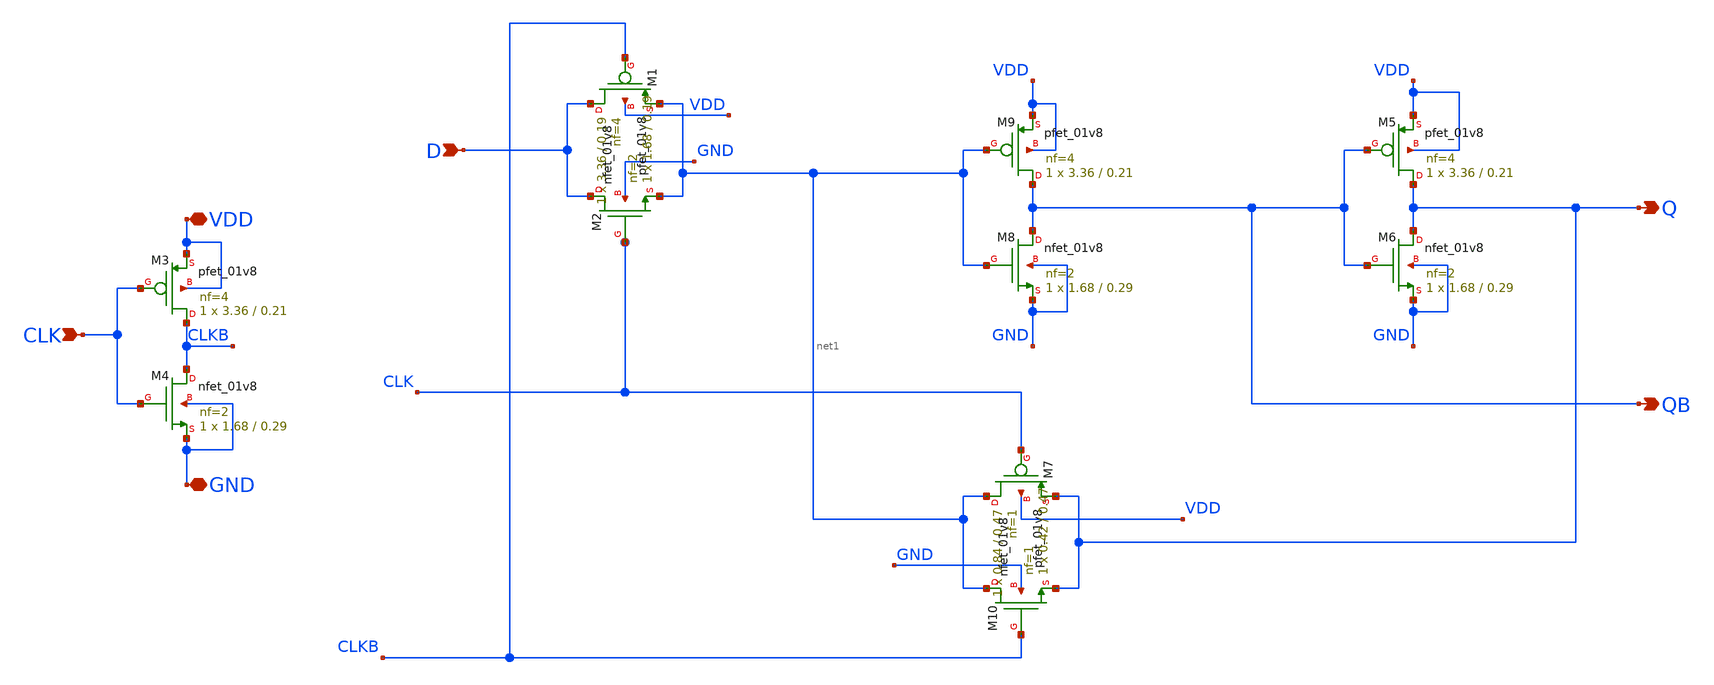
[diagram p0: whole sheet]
** sch_path: cells/DLX4/schematic/dlx4.sch
**.subckt dlx4 D VDD GND CLK QB Q
*.ipin D
*.iopin VDD
*.iopin GND
*.ipin CLK
*.opin QB
*.opin Q
XM1 D CLKB net1 VDD sky130_fd_pr__pfet_01v8 L=0.19 W=3.36 nf=4 ad='int((4 + 1)/2) * 3.36 / 4 * 0.29'
+ as='int((4 + 2)/2) * 3.36 / 4 * 0.29' pd='2*int((4 + 1)/2) * (3.36 / 4 + 0.29)' ps='2*int((4 + 2)/2) * (3.36 / 4 + 0.29)'
+ nrd='0.29 / 3.36 ' nrs='0.29 / 3.36 ' sa=0 sb=0 sd=0 mult=1 m=1
XM2 D CLK net1 GND sky130_fd_pr__nfet_01v8 L=0.19 W=1.68 nf=2 ad='int((2 + 1)/2) * 1.68 / 2 * 0.29' as='int((2 + 2)/2) * 1.68 / 2 * 0.29'
+ pd='2*int((2 + 1)/2) * (1.68 / 2 + 0.29)' ps='2*int((2 + 2)/2) * (1.68 / 2 + 0.29)' nrd='0.29 / 1.68 '
+ nrs='0.29 / 1.68 ' sa=0 sb=0 sd=0 mult=1 m=1
XM3 CLKB CLK VDD VDD sky130_fd_pr__pfet_01v8 L=0.21 W=3.36 nf=4 ad='int((4 + 1)/2) * 3.36 / 4 * 0.29'
+ as='int((4 + 2)/2) * 3.36 / 4 * 0.29' pd='2*int((4 + 1)/2) * (3.36 / 4 + 0.29)' ps='2*int((4 + 2)/2) * (3.36 / 4 + 0.29)'
+ nrd='0.29 / 3.36 ' nrs='0.29 / 3.36 ' sa=0 sb=0 sd=0 mult=1 m=1
XM4 CLKB CLK GND GND sky130_fd_pr__nfet_01v8 L=0.29 W=1.68 nf=2 ad='int((2 + 1)/2) * 1.68 / 2 * 0.29'
+ as='int((2 + 2)/2) * 1.68 / 2 * 0.29' pd='2*int((2 + 1)/2) * (1.68 / 2 + 0.29)' ps='2*int((2 + 2)/2) * (1.68 / 2 + 0.29)'
+ nrd='0.29 / 1.68 ' nrs='0.29 / 1.68 ' sa=0 sb=0 sd=0 mult=1 m=1
XM9 QB net1 VDD VDD sky130_fd_pr__pfet_01v8 L=0.21 W=3.36 nf=4 ad='int((4 + 1)/2) * 3.36 / 4 * 0.29'
+ as='int((4 + 2)/2) * 3.36 / 4 * 0.29' pd='2*int((4 + 1)/2) * (3.36 / 4 + 0.29)' ps='2*int((4 + 2)/2) * (3.36 / 4 + 0.29)'
+ nrd='0.29 / 3.36 ' nrs='0.29 / 3.36 ' sa=0 sb=0 sd=0 mult=1 m=1
XM8 QB net1 GND GND sky130_fd_pr__nfet_01v8 L=0.29 W=1.68 nf=2 ad='int((2 + 1)/2) * 1.68 / 2 * 0.29'
+ as='int((2 + 2)/2) * 1.68 / 2 * 0.29' pd='2*int((2 + 1)/2) * (1.68 / 2 + 0.29)' ps='2*int((2 + 2)/2) * (1.68 / 2 + 0.29)'
+ nrd='0.29 / 1.68 ' nrs='0.29 / 1.68 ' sa=0 sb=0 sd=0 mult=1 m=1
XM5 Q QB VDD VDD sky130_fd_pr__pfet_01v8 L=0.21 W=3.36 nf=4 ad='int((4 + 1)/2) * 3.36 / 4 * 0.29' as='int((4 + 2)/2) * 3.36 / 4 * 0.29'
+ pd='2*int((4 + 1)/2) * (3.36 / 4 + 0.29)' ps='2*int((4 + 2)/2) * (3.36 / 4 + 0.29)' nrd='0.29 / 3.36 '
+ nrs='0.29 / 3.36 ' sa=0 sb=0 sd=0 mult=1 m=1
XM6 Q QB GND GND sky130_fd_pr__nfet_01v8 L=0.29 W=1.68 nf=2 ad='int((2 + 1)/2) * 1.68 / 2 * 0.29' as='int((2 + 2)/2) * 1.68 / 2 * 0.29'
+ pd='2*int((2 + 1)/2) * (1.68 / 2 + 0.29)' ps='2*int((2 + 2)/2) * (1.68 / 2 + 0.29)' nrd='0.29 / 1.68 '
+ nrs='0.29 / 1.68 ' sa=0 sb=0 sd=0 mult=1 m=1
XM7 net1 CLK Q VDD sky130_fd_pr__pfet_01v8 L=0.47 W=0.84 nf=1 ad='int((1 + 1)/2) * 0.84 / 1 * 0.29' as='int((1 + 2)/2) * 0.84 / 1 * 0.29'
+ pd='2*int((1 + 1)/2) * (0.84 / 1 + 0.29)' ps='2*int((1 + 2)/2) * (0.84 / 1 + 0.29)' nrd='0.29 / 0.84 '
+ nrs='0.29 / 0.84 ' sa=0 sb=0 sd=0 mult=1 m=1
XM10 net1 CLKB Q GND sky130_fd_pr__nfet_01v8 L=0.47 W=0.42 nf=1 ad='int((1 + 1)/2) * 0.42 / 1 * 0.29'
+ as='int((1 + 2)/2) * 0.42 / 1 * 0.29' pd='2*int((1 + 1)/2) * (0.42 / 1 + 0.29)' ps='2*int((1 + 2)/2) * (0.42 / 1 + 0.29)'
+ nrd='0.29 / 0.42 ' nrs='0.29 / 0.42 ' sa=0 sb=0 sd=0 mult=1 m=1
**.ends
.end
